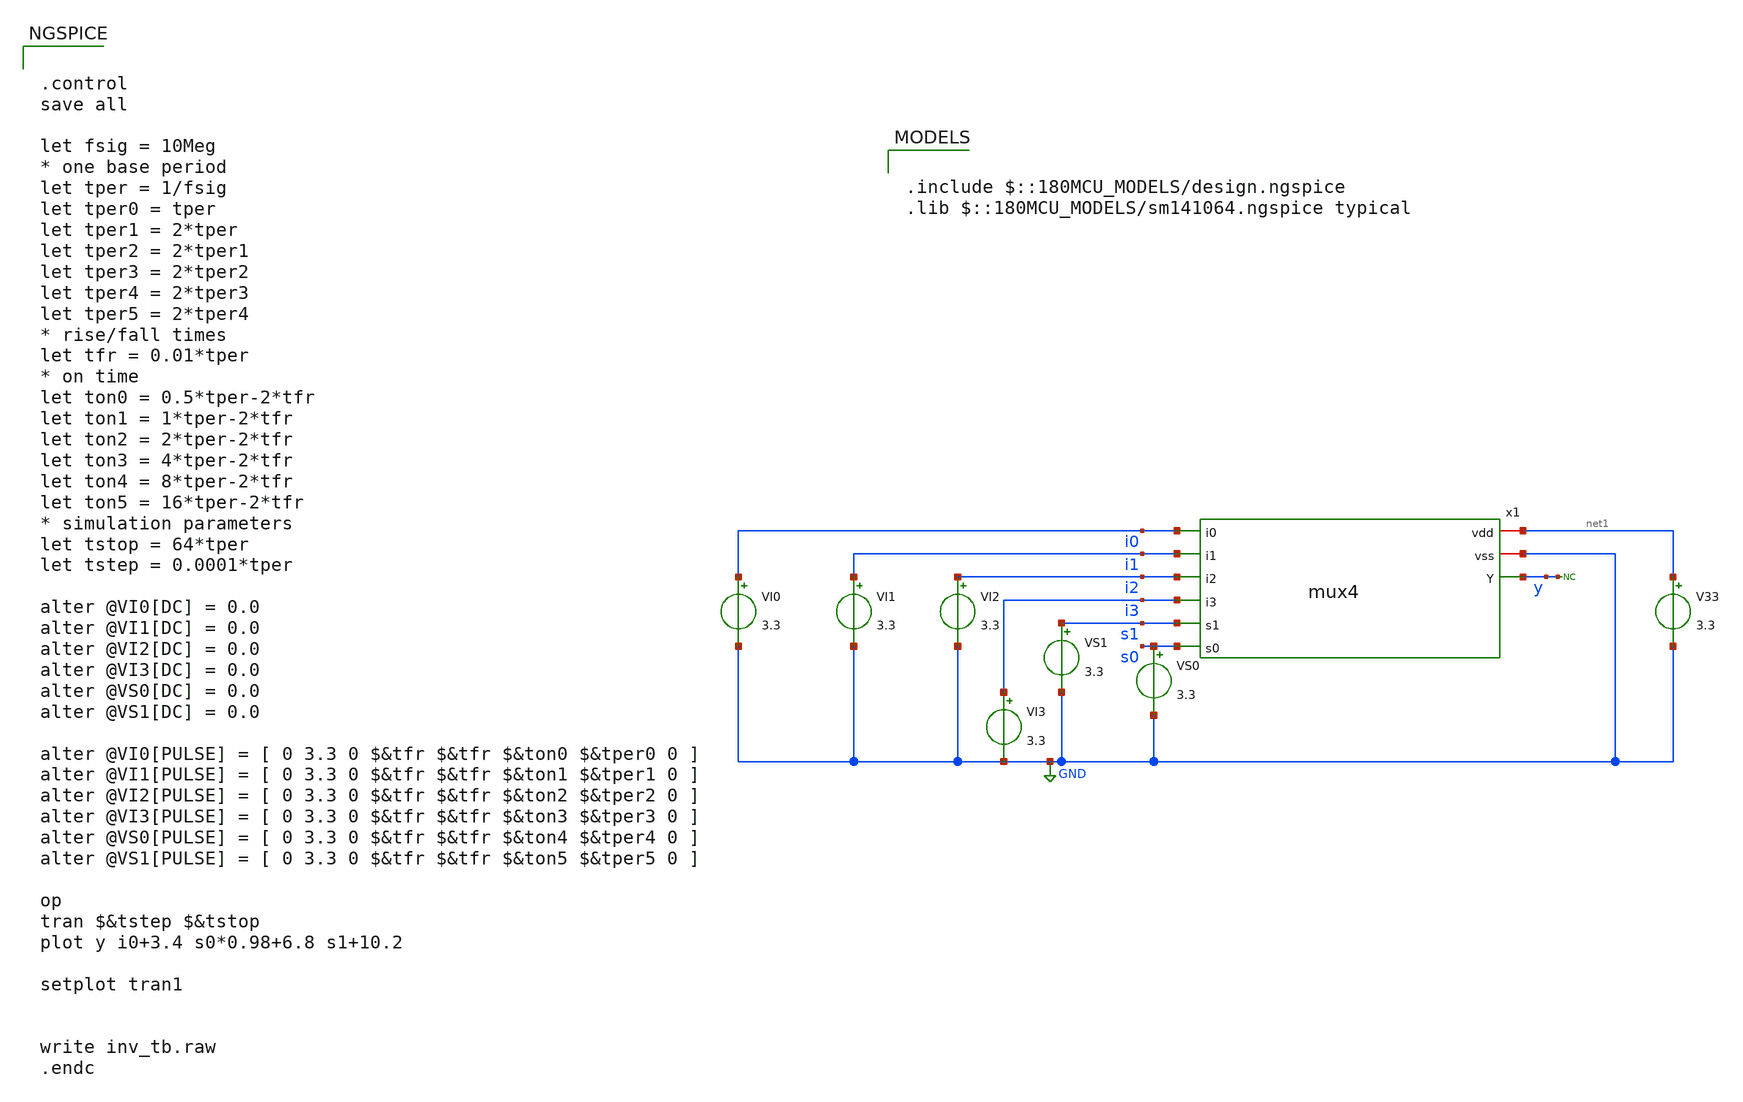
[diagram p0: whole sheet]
** sch_path: yuri-preliminary-work/mux4_tb.sch
**.subckt mux4_tb
V33 net1 GND 3.3
VI0 i0 GND 3.3
VI1 i1 GND 3.3
VI2 i2 GND 3.3
* noconn y
VS0 s0 GND 3.3
VS1 s1 GND 3.3
VI3 i3 GND 3.3
x1 net1 GND i0 i1 i2 i3 s1 s0 y mux4
**** begin user architecture code

.include $::180MCU_MODELS/design.ngspice
.lib $::180MCU_MODELS/sm141064.ngspice typical



.control
save all

let fsig = 10Meg
* one base period
let tper = 1/fsig
let tper0 = tper
let tper1 = 2*tper
let tper2 = 2*tper1
let tper3 = 2*tper2
let tper4 = 2*tper3
let tper5 = 2*tper4
* rise/fall times
let tfr = 0.01*tper
* on time
let ton0 = 0.5*tper-2*tfr
let ton1 = 1*tper-2*tfr
let ton2 = 2*tper-2*tfr
let ton3 = 4*tper-2*tfr
let ton4 = 8*tper-2*tfr
let ton5 = 16*tper-2*tfr
* simulation parameters
let tstop = 64*tper
let tstep = 0.0001*tper

alter @VI0[DC] = 0.0
alter @VI1[DC] = 0.0
alter @VI2[DC] = 0.0
alter @VI3[DC] = 0.0
alter @VS0[DC] = 0.0
alter @VS1[DC] = 0.0

alter @VI0[PULSE] = [ 0 3.3 0 $&tfr $&tfr $&ton0 $&tper0 0 ]
alter @VI1[PULSE] = [ 0 3.3 0 $&tfr $&tfr $&ton1 $&tper1 0 ]
alter @VI2[PULSE] = [ 0 3.3 0 $&tfr $&tfr $&ton2 $&tper2 0 ]
alter @VI3[PULSE] = [ 0 3.3 0 $&tfr $&tfr $&ton3 $&tper3 0 ]
alter @VS0[PULSE] = [ 0 3.3 0 $&tfr $&tfr $&ton4 $&tper4 0 ]
alter @VS1[PULSE] = [ 0 3.3 0 $&tfr $&tfr $&ton5 $&tper5 0 ]

op
tran $&tstep $&tstop
plot y i0+3.4 s0*0.98+6.8 s1+10.2

setplot tran1


write inv_tb.raw
.endc


**** end user architecture code
**.ends

* expanding   symbol:  stdcells/mux4/mux4.sym # of pins=9
** sym_path: yuri-preliminary-work/mux4.sym
** sch_path: yuri-preliminary-work/mux4.sch
.subckt mux4 vdd vss i0 i1 i2 i3 s1 s0 Y
*.iopin vss
*.iopin vdd
*.ipin i0
*.ipin i1
*.ipin i2
*.ipin i3
*.ipin s0
*.ipin s1
*.opin Y
XM1 net1 i0 vss vss nfet_03v3 L=0.3u W=0.85u nf=1 ad='int((nf+1)/2) * W/nf * 0.18u' as='int((nf+2)/2) * W/nf * 0.18u'
+ pd='2*int((nf+1)/2) * (W/nf + 0.18u)' ps='2*int((nf+2)/2) * (W/nf + 0.18u)' nrd='0.18u / W' nrs='0.18u / W'
+ sa=0 sb=0 sd=0 m=1
XM2 net1 i0 vdd vdd pfet_03v3 L=0.3u W=1.7u nf=1 ad='int((nf+1)/2) * W/nf * 0.18u' as='int((nf+2)/2) * W/nf * 0.18u'
+ pd='2*int((nf+1)/2) * (W/nf + 0.18u)' ps='2*int((nf+2)/2) * (W/nf + 0.18u)' nrd='0.18u / W' nrs='0.18u / W'
+ sa=0 sb=0 sd=0 m=1
XM3 net2 s0 net1 vdd pfet_03v3 L=0.3u W=1.7u nf=1 ad='int((nf+1)/2) * W/nf * 0.18u' as='int((nf+2)/2) * W/nf * 0.18u'
+ pd='2*int((nf+1)/2) * (W/nf + 0.18u)' ps='2*int((nf+2)/2) * (W/nf + 0.18u)' nrd='0.18u / W' nrs='0.18u / W'
+ sa=0 sb=0 sd=0 m=1
XM4 net2 s0_i net1 vss nfet_03v3 L=0.3u W=0.85u nf=1 ad='int((nf+1)/2) * W/nf * 0.18u' as='int((nf+2)/2) * W/nf * 0.18u'
+ pd='2*int((nf+1)/2) * (W/nf + 0.18u)' ps='2*int((nf+2)/2) * (W/nf + 0.18u)' nrd='0.18u / W' nrs='0.18u / W'
+ sa=0 sb=0 sd=0 m=1
XM5 net3 i1 vss vss nfet_03v3 L=0.3u W=0.85u nf=1 ad='int((nf+1)/2) * W/nf * 0.18u' as='int((nf+2)/2) * W/nf * 0.18u'
+ pd='2*int((nf+1)/2) * (W/nf + 0.18u)' ps='2*int((nf+2)/2) * (W/nf + 0.18u)' nrd='0.18u / W' nrs='0.18u / W'
+ sa=0 sb=0 sd=0 m=1
XM6 net3 i1 vdd vdd pfet_03v3 L=0.3u W=1.7u nf=1 ad='int((nf+1)/2) * W/nf * 0.18u' as='int((nf+2)/2) * W/nf * 0.18u'
+ pd='2*int((nf+1)/2) * (W/nf + 0.18u)' ps='2*int((nf+2)/2) * (W/nf + 0.18u)' nrd='0.18u / W' nrs='0.18u / W'
+ sa=0 sb=0 sd=0 m=1
XM7 net2 s0_i net3 vdd pfet_03v3 L=0.3u W=1.7u nf=1 ad='int((nf+1)/2) * W/nf * 0.18u' as='int((nf+2)/2) * W/nf * 0.18u'
+ pd='2*int((nf+1)/2) * (W/nf + 0.18u)' ps='2*int((nf+2)/2) * (W/nf + 0.18u)' nrd='0.18u / W' nrs='0.18u / W'
+ sa=0 sb=0 sd=0 m=1
XM8 net2 s0 net3 vss nfet_03v3 L=0.3u W=0.85u nf=1 ad='int((nf+1)/2) * W/nf * 0.18u' as='int((nf+2)/2) * W/nf * 0.18u'
+ pd='2*int((nf+1)/2) * (W/nf + 0.18u)' ps='2*int((nf+2)/2) * (W/nf + 0.18u)' nrd='0.18u / W' nrs='0.18u / W'
+ sa=0 sb=0 sd=0 m=1
XM11 net4 i2 vss vss nfet_03v3 L=0.3u W=0.85u nf=1 ad='int((nf+1)/2) * W/nf * 0.18u' as='int((nf+2)/2) * W/nf * 0.18u'
+ pd='2*int((nf+1)/2) * (W/nf + 0.18u)' ps='2*int((nf+2)/2) * (W/nf + 0.18u)' nrd='0.18u / W' nrs='0.18u / W'
+ sa=0 sb=0 sd=0 m=1
XM12 net4 i2 vdd vdd pfet_03v3 L=0.3u W=1.7u nf=1 ad='int((nf+1)/2) * W/nf * 0.18u' as='int((nf+2)/2) * W/nf * 0.18u'
+ pd='2*int((nf+1)/2) * (W/nf + 0.18u)' ps='2*int((nf+2)/2) * (W/nf + 0.18u)' nrd='0.18u / W' nrs='0.18u / W'
+ sa=0 sb=0 sd=0 m=1
XM13 net5 s0 net4 vdd pfet_03v3 L=0.3u W=1.7u nf=1 ad='int((nf+1)/2) * W/nf * 0.18u' as='int((nf+2)/2) * W/nf * 0.18u'
+ pd='2*int((nf+1)/2) * (W/nf + 0.18u)' ps='2*int((nf+2)/2) * (W/nf + 0.18u)' nrd='0.18u / W' nrs='0.18u / W'
+ sa=0 sb=0 sd=0 m=1
XM14 net5 s0_i net4 vss nfet_03v3 L=0.3u W=0.85u nf=1 ad='int((nf+1)/2) * W/nf * 0.18u' as='int((nf+2)/2) * W/nf * 0.18u'
+ pd='2*int((nf+1)/2) * (W/nf + 0.18u)' ps='2*int((nf+2)/2) * (W/nf + 0.18u)' nrd='0.18u / W' nrs='0.18u / W'
+ sa=0 sb=0 sd=0 m=1
XM15 net6 i3 vss vss nfet_03v3 L=0.3u W=0.85u nf=1 ad='int((nf+1)/2) * W/nf * 0.18u' as='int((nf+2)/2) * W/nf * 0.18u'
+ pd='2*int((nf+1)/2) * (W/nf + 0.18u)' ps='2*int((nf+2)/2) * (W/nf + 0.18u)' nrd='0.18u / W' nrs='0.18u / W'
+ sa=0 sb=0 sd=0 m=1
XM16 net6 i3 vdd vdd pfet_03v3 L=0.3u W=1.7u nf=1 ad='int((nf+1)/2) * W/nf * 0.18u' as='int((nf+2)/2) * W/nf * 0.18u'
+ pd='2*int((nf+1)/2) * (W/nf + 0.18u)' ps='2*int((nf+2)/2) * (W/nf + 0.18u)' nrd='0.18u / W' nrs='0.18u / W'
+ sa=0 sb=0 sd=0 m=1
XM17 net5 s0_i net6 vdd pfet_03v3 L=0.3u W=1.7u nf=1 ad='int((nf+1)/2) * W/nf * 0.18u' as='int((nf+2)/2) * W/nf * 0.18u'
+ pd='2*int((nf+1)/2) * (W/nf + 0.18u)' ps='2*int((nf+2)/2) * (W/nf + 0.18u)' nrd='0.18u / W' nrs='0.18u / W'
+ sa=0 sb=0 sd=0 m=1
XM18 net5 s0 net6 vss nfet_03v3 L=0.3u W=0.85u nf=1 ad='int((nf+1)/2) * W/nf * 0.18u' as='int((nf+2)/2) * W/nf * 0.18u'
+ pd='2*int((nf+1)/2) * (W/nf + 0.18u)' ps='2*int((nf+2)/2) * (W/nf + 0.18u)' nrd='0.18u / W' nrs='0.18u / W'
+ sa=0 sb=0 sd=0 m=1
XM9 Y_i s1 net2 vdd pfet_03v3 L=0.3u W=1.7u nf=1 ad='int((nf+1)/2) * W/nf * 0.18u' as='int((nf+2)/2) * W/nf * 0.18u'
+ pd='2*int((nf+1)/2) * (W/nf + 0.18u)' ps='2*int((nf+2)/2) * (W/nf + 0.18u)' nrd='0.18u / W' nrs='0.18u / W'
+ sa=0 sb=0 sd=0 m=1
XM10 Y_i s1_i net2 vss nfet_03v3 L=0.3u W=0.85u nf=1 ad='int((nf+1)/2) * W/nf * 0.18u' as='int((nf+2)/2) * W/nf * 0.18u'
+ pd='2*int((nf+1)/2) * (W/nf + 0.18u)' ps='2*int((nf+2)/2) * (W/nf + 0.18u)' nrd='0.18u / W' nrs='0.18u / W'
+ sa=0 sb=0 sd=0 m=1
XM19 Y_i s1_i net5 vdd pfet_03v3 L=0.3u W=1.7u nf=1 ad='int((nf+1)/2) * W/nf * 0.18u' as='int((nf+2)/2) * W/nf * 0.18u'
+ pd='2*int((nf+1)/2) * (W/nf + 0.18u)' ps='2*int((nf+2)/2) * (W/nf + 0.18u)' nrd='0.18u / W' nrs='0.18u / W'
+ sa=0 sb=0 sd=0 m=1
XM20 Y_i s1 net5 vss nfet_03v3 L=0.3u W=0.85u nf=1 ad='int((nf+1)/2) * W/nf * 0.18u' as='int((nf+2)/2) * W/nf * 0.18u'
+ pd='2*int((nf+1)/2) * (W/nf + 0.18u)' ps='2*int((nf+2)/2) * (W/nf + 0.18u)' nrd='0.18u / W' nrs='0.18u / W'
+ sa=0 sb=0 sd=0 m=1
XM21 s0_i s0 vdd vdd pfet_03v3 L=0.3u W=1.7u nf=1 ad='int((nf+1)/2) * W/nf * 0.18u' as='int((nf+2)/2) * W/nf * 0.18u'
+ pd='2*int((nf+1)/2) * (W/nf + 0.18u)' ps='2*int((nf+2)/2) * (W/nf + 0.18u)' nrd='0.18u / W' nrs='0.18u / W'
+ sa=0 sb=0 sd=0 m=1
XM22 s0_i s0 vss vss nfet_03v3 L=0.3u W=0.85u nf=1 ad='int((nf+1)/2) * W/nf * 0.18u' as='int((nf+2)/2) * W/nf * 0.18u'
+ pd='2*int((nf+1)/2) * (W/nf + 0.18u)' ps='2*int((nf+2)/2) * (W/nf + 0.18u)' nrd='0.18u / W' nrs='0.18u / W'
+ sa=0 sb=0 sd=0 m=1
XM23 s1_i s1 vdd vdd pfet_03v3 L=0.3u W=1.7u nf=1 ad='int((nf+1)/2) * W/nf * 0.18u' as='int((nf+2)/2) * W/nf * 0.18u'
+ pd='2*int((nf+1)/2) * (W/nf + 0.18u)' ps='2*int((nf+2)/2) * (W/nf + 0.18u)' nrd='0.18u / W' nrs='0.18u / W'
+ sa=0 sb=0 sd=0 m=1
XM24 s1_i s1 vss vss nfet_03v3 L=0.3u W=0.85u nf=1 ad='int((nf+1)/2) * W/nf * 0.18u' as='int((nf+2)/2) * W/nf * 0.18u'
+ pd='2*int((nf+1)/2) * (W/nf + 0.18u)' ps='2*int((nf+2)/2) * (W/nf + 0.18u)' nrd='0.18u / W' nrs='0.18u / W'
+ sa=0 sb=0 sd=0 m=1
XM25 Y Y_i vdd vdd pfet_03v3 L=0.3u W=1.7u nf=1 ad='int((nf+1)/2) * W/nf * 0.18u' as='int((nf+2)/2) * W/nf * 0.18u'
+ pd='2*int((nf+1)/2) * (W/nf + 0.18u)' ps='2*int((nf+2)/2) * (W/nf + 0.18u)' nrd='0.18u / W' nrs='0.18u / W'
+ sa=0 sb=0 sd=0 m=1
XM26 Y Y_i vss vss nfet_03v3 L=0.3u W=0.85u nf=1 ad='int((nf+1)/2) * W/nf * 0.18u' as='int((nf+2)/2) * W/nf * 0.18u'
+ pd='2*int((nf+1)/2) * (W/nf + 0.18u)' ps='2*int((nf+2)/2) * (W/nf + 0.18u)' nrd='0.18u / W' nrs='0.18u / W'
+ sa=0 sb=0 sd=0 m=1
.ends

.GLOBAL GND
.end
